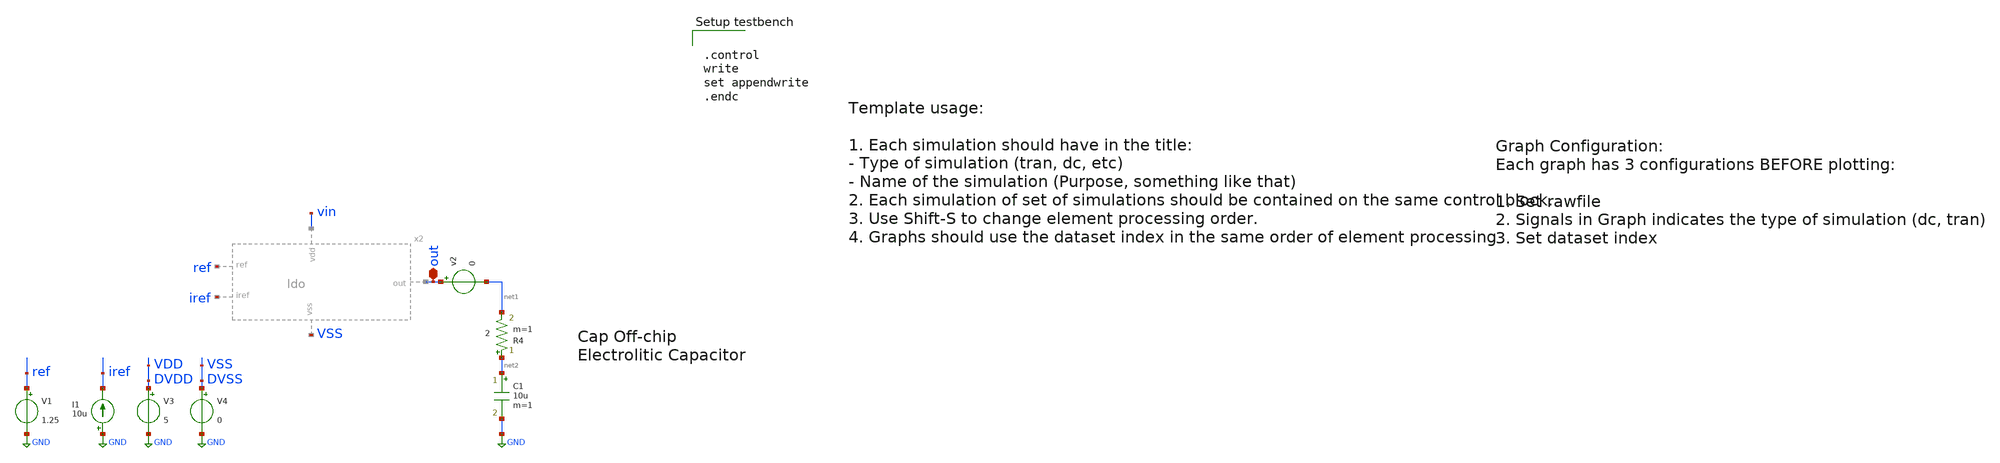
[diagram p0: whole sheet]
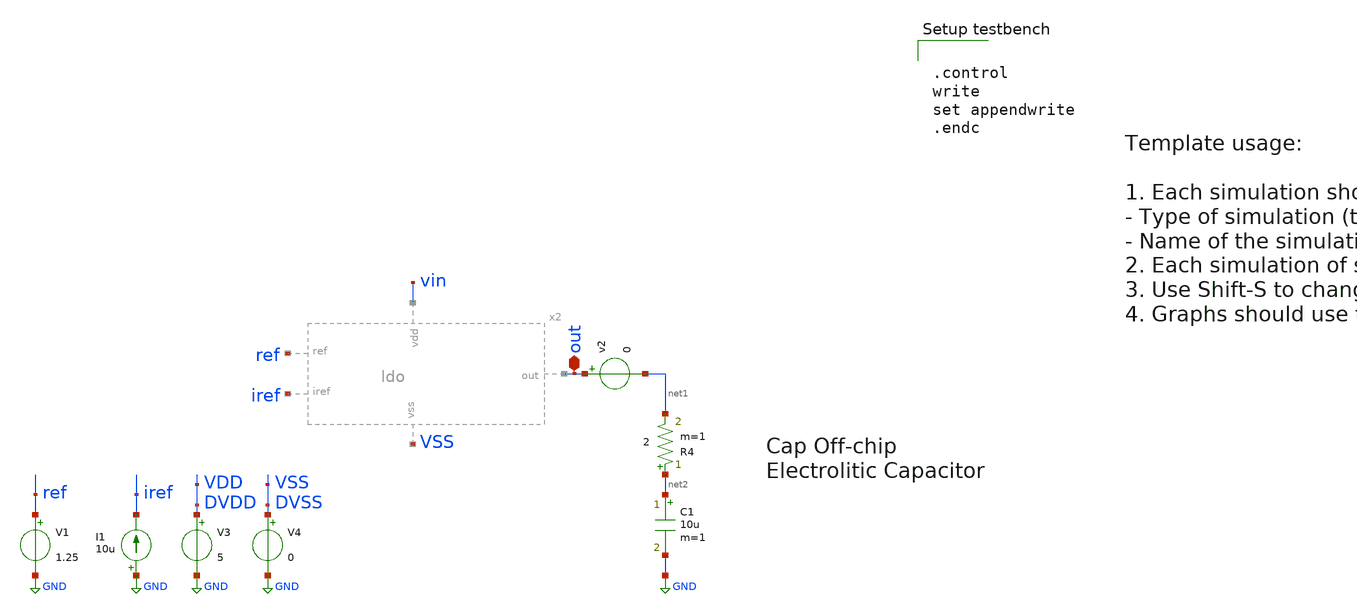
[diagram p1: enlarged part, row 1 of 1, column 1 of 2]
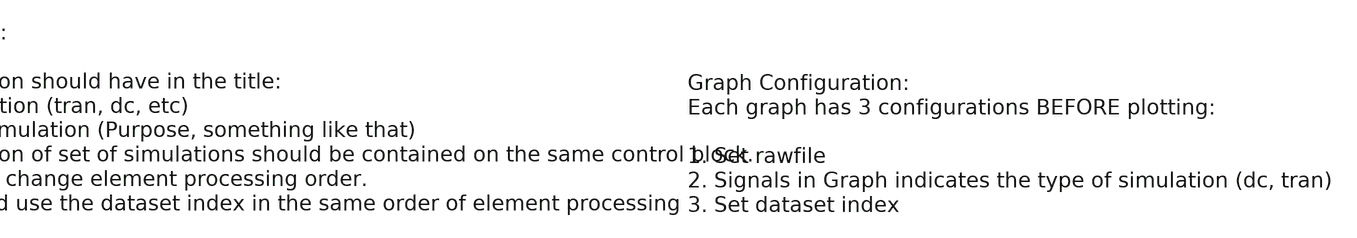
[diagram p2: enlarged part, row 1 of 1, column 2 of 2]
** sch_path: LDO/xschem/ldo/test/line_regulation.sch

.include $env(PDK_ROOT)/$env(PDK)/libs.tech/ngspice/design.ngspice
.lib $env(PDK_ROOT)/$env(PDK)/libs.tech/ngspice/sm141064.ngspice typical
.lib $env(PDK_ROOT)/$env(PDK)/libs.tech/ngspice/sm141064.ngspice res_typical
.lib $env(PDK_ROOT)/$env(PDK)/libs.tech/ngspice/sm141064.ngspice diode_typical
.lib $env(PDK_ROOT)/$env(PDK)/libs.tech/ngspice/sm141064.ngspice bjt_typical
.lib $env(PDK_ROOT)/$env(PDK)/libs.tech/ngspice/sm141064.ngspice cap_mim
.lib $env(PDK_ROOT)/$env(PDK)/libs.tech/ngspice/sm141064.ngspice moscap_typical
.lib $env(PDK_ROOT)/$env(PDK)/libs.tech/ngspice/sm141064.ngspice mimcap_typical

.include $env(PDK_ROOT)/$env(PDK)/libs.ref/gf180mcu_fd_io/spice/gf180mcu_fd_io.spice


.control
write
set appendwrite
.endc


**.subckt line_regulation out
*.iopin out
I1 GND iref 10u
V1 ref GND 1.25
v2 out net1 0
C1 net2 GND 10u m=1
R4 net2 net1 2 m=1
V3 DVDD GND 5
V4 DVSS GND 0
**** begin user architecture code


.param R=33
R10 out 0 {R}
IL out 0 PWL(0 0.1m 10u 0.1m 20u 10m 30u 10m)

Vs vin 0 5

.nodeset v(out)=0
.nodeset v(x2.feedback)=0
.nodeset v(out)=3.3
.nodeset v(x2.op_out)=0

*supply_sweep
.control
save vin out
alter IL 0
dc Vs 6 0 -0.01
plot v(vin) v(out)
meas DC vldo_sup_4_6 FIND v(out) AT=4.6
meas DC vldo_nom FIND v(out) AT=5
meas DC vldo_sup_5_4 FIND v(out) AT=5.4
let line_reg = abs((vldo_sup_5_4-vldo_sup_4_6)/0.8)
print line_reg
meas DC vin WHEN v(out)=3.2982
let dropout = vin-3.2982
print dropout

write
.endc




.include ../../../spice/ldo_pex.spice
**** iref out ref vss vdd ldo_pex
x2   iref out ref GND vin ldo_pex


**** end user architecture code
**.ends
.GLOBAL GND
.end
